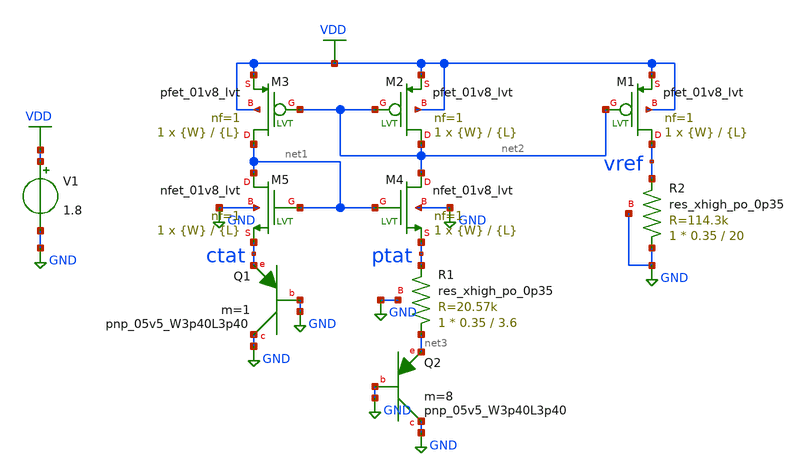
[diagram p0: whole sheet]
** sch_path: xschem/ptat.sch
**.subckt ptat
V1 VDD GND 1.8
XQ1 GND GND ctat sky130_fd_pr__pnp_05v5_W3p40L3p40 m=1
XQ2 GND GND net3 sky130_fd_pr__pnp_05v5_W3p40L3p40 m=8
XR1 net3 ptat GND sky130_fd_pr__res_xhigh_po_0p35 L=3.6 mult=1 m=1
XR2 GND vref GND sky130_fd_pr__res_xhigh_po_0p35 L=20 mult=1 m=1
XM1 vref net2 VDD VDD sky130_fd_pr__pfet_01v8_lvt L={L} W={W} nf=1 ad='int((nf+1)/2) * W/nf * 0.29' as='int((nf+2)/2) * W/nf * 0.29'
+ pd='2*int((nf+1)/2) * (W/nf + 0.29)' ps='2*int((nf+2)/2) * (W/nf + 0.29)' nrd='0.29 / W' nrs='0.29 / W'
+ sa=0 sb=0 sd=0 mult=1 m=1
XM2 net2 net2 VDD VDD sky130_fd_pr__pfet_01v8_lvt L={L} W={W} nf=1 ad='int((nf+1)/2) * W/nf * 0.29' as='int((nf+2)/2) * W/nf * 0.29'
+ pd='2*int((nf+1)/2) * (W/nf + 0.29)' ps='2*int((nf+2)/2) * (W/nf + 0.29)' nrd='0.29 / W' nrs='0.29 / W'
+ sa=0 sb=0 sd=0 mult=1 m=1
XM3 net1 net2 VDD VDD sky130_fd_pr__pfet_01v8_lvt L={L} W={W} nf=1 ad='int((nf+1)/2) * W/nf * 0.29' as='int((nf+2)/2) * W/nf * 0.29'
+ pd='2*int((nf+1)/2) * (W/nf + 0.29)' ps='2*int((nf+2)/2) * (W/nf + 0.29)' nrd='0.29 / W' nrs='0.29 / W'
+ sa=0 sb=0 sd=0 mult=1 m=1
XM4 net2 net1 ptat GND sky130_fd_pr__nfet_01v8_lvt L={L} W={W} nf=1 ad='int((nf+1)/2) * W/nf * 0.29'
+ as='int((nf+2)/2) * W/nf * 0.29' pd='2*int((nf+1)/2) * (W/nf + 0.29)' ps='2*int((nf+2)/2) * (W/nf + 0.29)'
+ nrd='0.29 / W' nrs='0.29 / W' sa=0 sb=0 sd=0 mult=1 m=1
XM5 net1 net1 ctat GND sky130_fd_pr__nfet_01v8_lvt L={L} W={W} nf=1 ad='int((nf+1)/2) * W/nf * 0.29'
+ as='int((nf+2)/2) * W/nf * 0.29' pd='2*int((nf+1)/2) * (W/nf + 0.29)' ps='2*int((nf+2)/2) * (W/nf + 0.29)'
+ nrd='0.29 / W' nrs='0.29 / W' sa=0 sb=0 sd=0 mult=1 m=1
**** begin user architecture code

** opencircuitdesign pdks install
.lib $::SKYWATER_MODELS/sky130.lib.spice tt




.param L=1
.param W=50




** Analysis Requests **
** Outputs Requests **
.option wnflag=1
.option savecurrents
.control
save all
dc temp -40 125 5
plot ctat-ptat
plot vref
op
save all
write ptat.raw
.endc


**** end user architecture code
**.ends
.GLOBAL VDD
.GLOBAL GND
.end
